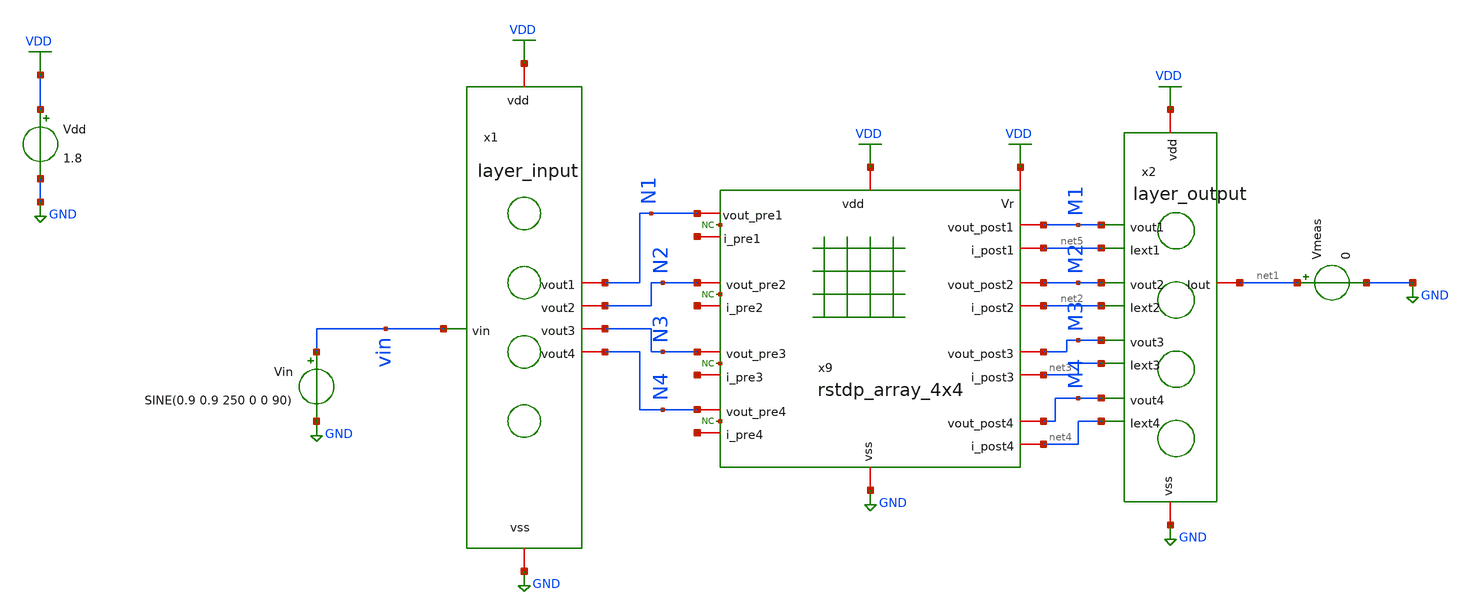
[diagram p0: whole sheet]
** sch_path: tb_4x4_modular_spice.sch
**.subckt tb_4x4_modular_spice
Vdd VDD GND 1.8
Vin vin GND SINE(0.9 0.9 250 0 0 90)
x9 VDD VDD net2 net5 M2 net3 GND M1 M3 net4 M4 N1 net6 N2 net7 N3 net8 N4 net9 rstdp_array_4x4
Vmeas net1 GND 0
x1 VDD GND vin N1 N2 N3 N4 layer_input
x2 VDD net5 GND net2 net3 net1 net4 M1 M2 M3 M4 layer_output
* noconn #net10
* noconn #net11
* noconn #net12
* noconn #net13
**** begin user architecture code
.lib $::SKYWATER_MODELS/sky130.lib.spice tt

** opencircuitdesign pdks install
*.inc $::SKYWATER_MODELS/rram_v0.spice
.inc /home/alex/Desktop/EDA/SNN_IPN/memristor_models/wellposed_spice/wllpsd.spice

**** end user architecture code
**.ends
.GLOBAL GND
.GLOBAL VDD
**** begin user architecture code


.option klu
.options num_threads=8
.tran 1u 5m uic
.control
	run
	write tb_4x4_modular_spice.raw
.endc


**** end user architecture code
.end
